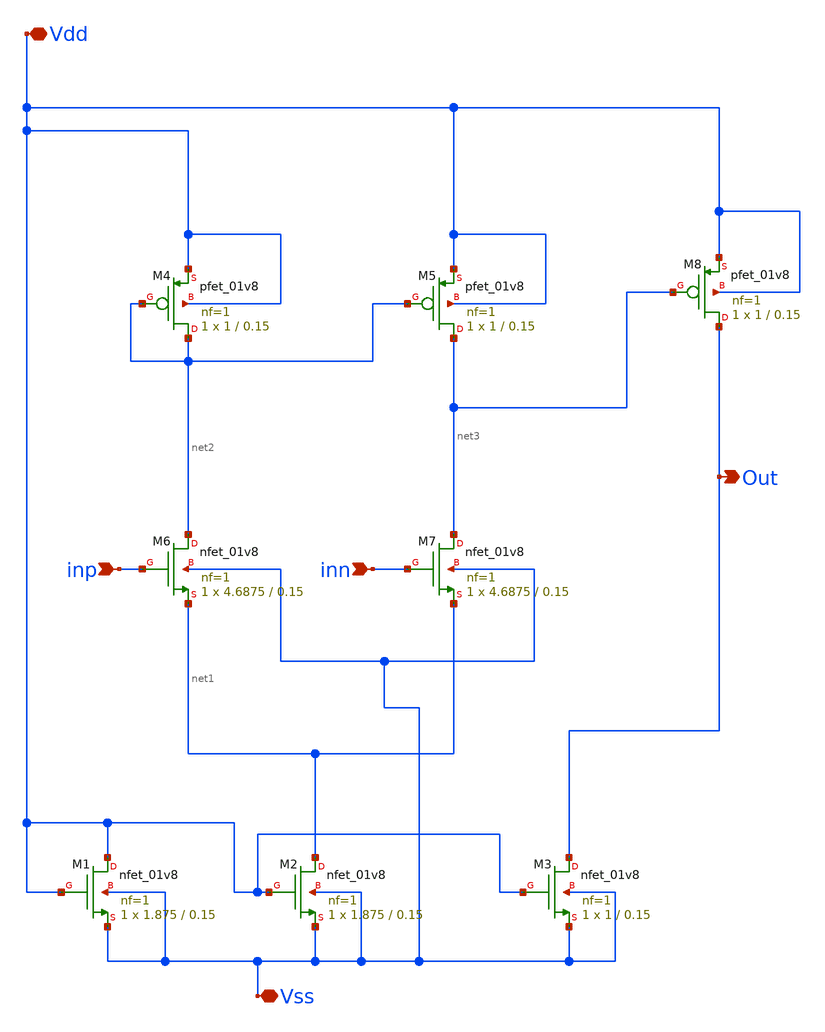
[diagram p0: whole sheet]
** sch_path: xschem/src/hw2_opamp1.sch
**.subckt hw2_opamp1 Vss Vdd inp inn Out
*.iopin Vss
*.iopin Vdd
*.ipin inp
*.ipin inn
*.opin Out
XM1 Vdd Vdd Vss Vss sky130_fd_pr__nfet_01v8 L=0.15 W=1.875 nf=1 ad='int((nf+1)/2) * W/nf * 0.29' as='int((nf+2)/2) * W/nf * 0.29'
+ pd='2*int((nf+1)/2) * (W/nf + 0.29)' ps='2*int((nf+2)/2) * (W/nf + 0.29)' nrd='0.29 / W' nrs='0.29 / W'
+ sa=0 sb=0 sd=0 mult=1 m=1
XM2 net1 Vdd Vss Vss sky130_fd_pr__nfet_01v8 L=0.15 W=1.875 nf=1 ad='int((nf+1)/2) * W/nf * 0.29' as='int((nf+2)/2) * W/nf * 0.29'
+ pd='2*int((nf+1)/2) * (W/nf + 0.29)' ps='2*int((nf+2)/2) * (W/nf + 0.29)' nrd='0.29 / W' nrs='0.29 / W'
+ sa=0 sb=0 sd=0 mult=1 m=1
XM3 Out Vdd Vss Vss sky130_fd_pr__nfet_01v8 L=0.15 W=1 nf=1 ad='int((nf+1)/2) * W/nf * 0.29' as='int((nf+2)/2) * W/nf * 0.29'
+ pd='2*int((nf+1)/2) * (W/nf + 0.29)' ps='2*int((nf+2)/2) * (W/nf + 0.29)' nrd='0.29 / W' nrs='0.29 / W'
+ sa=0 sb=0 sd=0 mult=1 m=1
XM4 net2 net2 Vdd Vdd sky130_fd_pr__pfet_01v8 L=0.15 W=1 nf=1 ad='int((nf+1)/2) * W/nf * 0.29' as='int((nf+2)/2) * W/nf * 0.29'
+ pd='2*int((nf+1)/2) * (W/nf + 0.29)' ps='2*int((nf+2)/2) * (W/nf + 0.29)' nrd='0.29 / W' nrs='0.29 / W'
+ sa=0 sb=0 sd=0 mult=1 m=1
XM5 net3 net2 Vdd Vdd sky130_fd_pr__pfet_01v8 L=0.15 W=1 nf=1 ad='int((nf+1)/2) * W/nf * 0.29' as='int((nf+2)/2) * W/nf * 0.29'
+ pd='2*int((nf+1)/2) * (W/nf + 0.29)' ps='2*int((nf+2)/2) * (W/nf + 0.29)' nrd='0.29 / W' nrs='0.29 / W'
+ sa=0 sb=0 sd=0 mult=1 m=1
XM6 net2 inp net1 Vss sky130_fd_pr__nfet_01v8 L=0.15 W=4.6875 nf=1 ad='int((nf+1)/2) * W/nf * 0.29' as='int((nf+2)/2) * W/nf * 0.29'
+ pd='2*int((nf+1)/2) * (W/nf + 0.29)' ps='2*int((nf+2)/2) * (W/nf + 0.29)' nrd='0.29 / W' nrs='0.29 / W'
+ sa=0 sb=0 sd=0 mult=1 m=1
XM7 net3 inn net1 Vss sky130_fd_pr__nfet_01v8 L=0.15 W=4.6875 nf=1 ad='int((nf+1)/2) * W/nf * 0.29' as='int((nf+2)/2) * W/nf * 0.29'
+ pd='2*int((nf+1)/2) * (W/nf + 0.29)' ps='2*int((nf+2)/2) * (W/nf + 0.29)' nrd='0.29 / W' nrs='0.29 / W'
+ sa=0 sb=0 sd=0 mult=1 m=1
XM8 Out net3 Vdd Vdd sky130_fd_pr__pfet_01v8 L=0.15 W=1 nf=1 ad='int((nf+1)/2) * W/nf * 0.29' as='int((nf+2)/2) * W/nf * 0.29'
+ pd='2*int((nf+1)/2) * (W/nf + 0.29)' ps='2*int((nf+2)/2) * (W/nf + 0.29)' nrd='0.29 / W' nrs='0.29 / W'
+ sa=0 sb=0 sd=0 mult=1 m=1
**.ends
.end
